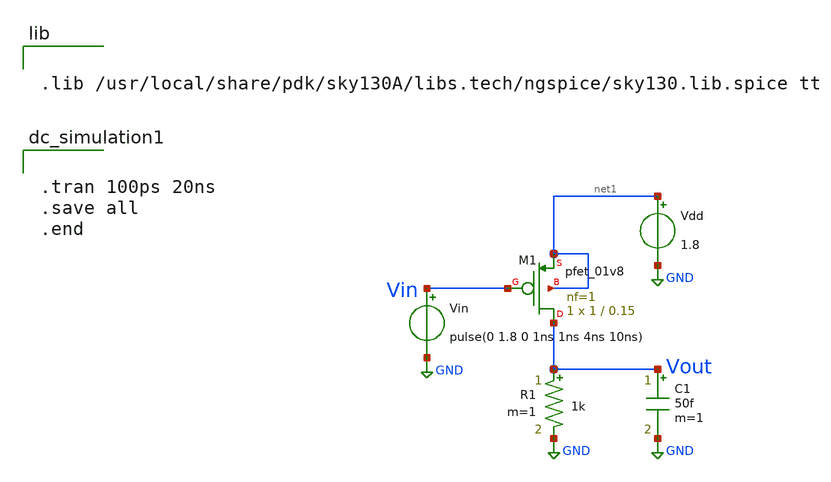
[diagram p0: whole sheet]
** sch_path: xschem/pmos.sch
**.subckt pmos
Vin Vin GND pulse(0 1.8 0 1ns 1ns 4ns 10ns)
Vdd net1 GND 1.8
XM1 Vout Vin net1 net1 sky130_fd_pr__pfet_01v8 L=0.15 W=1 nf=1 ad='int((nf+1)/2) * W/nf * 0.29' as='int((nf+2)/2) * W/nf * 0.29'
+ pd='2*int((nf+1)/2) * (W/nf + 0.29)' ps='2*int((nf+2)/2) * (W/nf + 0.29)' nrd='0.29 / W' nrs='0.29 / W'
+ sa=0 sb=0 sd=0 mult=1 m=1
R1 Vout GND 1k m=1
C1 Vout GND 50f m=1
**** begin user architecture code


.lib /usr/local/share/pdk/sky130A/libs.tech/ngspice/sky130.lib.spice tt




.tran 100ps 20ns
.save all
.end


**** end user architecture code
**.ends
.GLOBAL GND
.end
